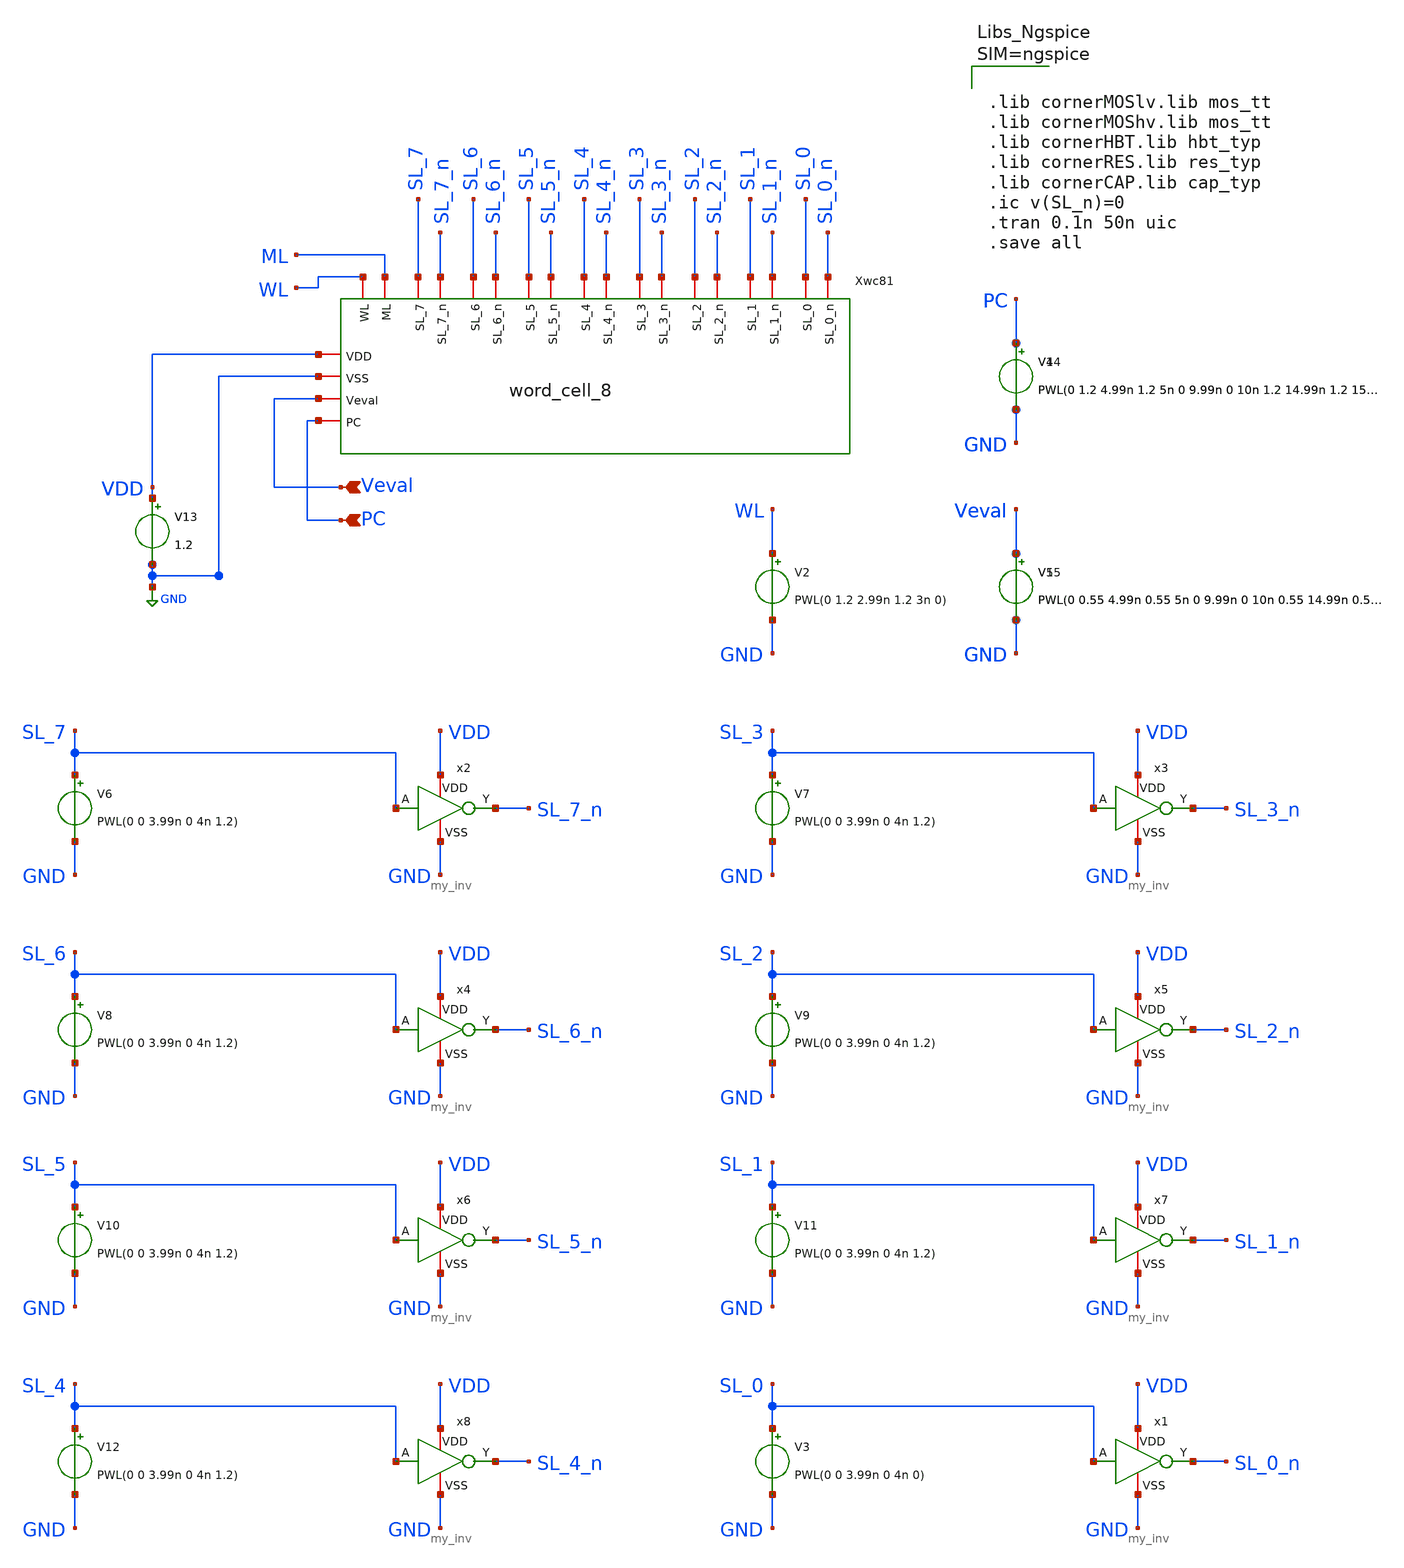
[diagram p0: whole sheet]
** sch_path: xschem/word_cell_8_TB.sch
**.subckt word_cell_8_TB PC Veval
*.ipin PC
*.ipin Veval
Xwc81 SL_3_n SL_1_n SL_2_n SL_0_n SL_7 SL_6 SL_5 SL_4 SL_3 SL_2 SL_1 SL_0 SL_7_n SL_6_n SL_5_n
+ SL_4_n WL ML VDD Veval GND PC word_cell_8
V1 VDD GND 1.2
V4 PC GND PWL(0 1.2 4.99n 1.2 5n 0 9.99n 0 10n 1.2 14.99n 1.2 15n 0 19.99n 0 20n 1.2 24.99n 1.2 25n
+ 0 29.99n 0 30n 1.2 34.99n 1.2 35n 0 39.99n 0 40n 1.2)
V5 Veval GND PWL(0 0.55 4.99n 0.55 5n 0 9.99n 0 10n 0.55 14.99n 0.55 15n 0 19.99n 0 20n 0.5 24.99n
+ 0.5 25n 0 29.99n 0 30n 0.6 34.99n 0.6 35n 0 39.99n 0 40n 0.6)
V3 SL_0 GND PWL(0 0 3.99n 0 4n 0)
V2 WL GND PWL(0 1.2 2.99n 1.2 3n 0)
x1 VDD SL_0_n SL_0 GND my_inv
V6 SL_7 GND PWL(0 0 3.99n 0 4n 1.2)
x2 VDD SL_7_n SL_7 GND my_inv
V7 SL_3 GND PWL(0 0 3.99n 0 4n 1.2)
x3 VDD SL_3_n SL_3 GND my_inv
V8 SL_6 GND PWL(0 0 3.99n 0 4n 1.2)
x4 VDD SL_6_n SL_6 GND my_inv
V9 SL_2 GND PWL(0 0 3.99n 0 4n 1.2)
x5 VDD SL_2_n SL_2 GND my_inv
V10 SL_5 GND PWL(0 0 3.99n 0 4n 1.2)
x6 VDD SL_5_n SL_5 GND my_inv
V11 SL_1 GND PWL(0 0 3.99n 0 4n 1.2)
x7 VDD SL_1_n SL_1 GND my_inv
V12 SL_4 GND PWL(0 0 3.99n 0 4n 1.2)
x8 VDD SL_4_n SL_4 GND my_inv
V13 VDD GND 1.2
V14 PC GND PWL(0 1.2 4.99n 1.2 5n 0 9.99n 0 10n 1.2 14.99n 1.2 15n 0 19.99n 0 20n 1.2 24.99n 1.2 25n
+ 0 29.99n 0 30n 1.2 34.99n 1.2 35n 0 39.99n 0 40n 1.2)
V15 Veval GND PWL(0 0.55 4.99n 0.55 5n 0 9.99n 0 10n 0.55 14.99n 0.55 15n 0 19.99n 0 20n 0.5 24.99n
+ 0.5 25n 0 29.99n 0 30n 0.6 34.99n 0.6 35n 0 39.99n 0 40n 0.6)
**** begin user architecture code



.lib cornerMOSlv.lib mos_tt
.lib cornerMOShv.lib mos_tt
.lib cornerHBT.lib hbt_typ
.lib cornerRES.lib res_typ
.lib cornerCAP.lib cap_typ
.ic v(SL_n)=0
.tran 0.1n 50n uic
.save all



**** end user architecture code
**.ends

* expanding   symbol:  word_cell_8.sym # of pins=22
** sym_path: xschem/word_cell_8.sym
** sch_path: xschem/word_cell_8.sch
.subckt word_cell_8 SL_3_n SL_1_n SL_2_n SL_0_n SL_7 SL_6 SL_5 SL_4 SL_3 SL_2 SL_1 SL_0 SL_7_n
+ SL_6_n SL_5_n SL_4_n WL ML VDD Veval VSS PC
*.iopin VSS
*.iopin Veval
*.iopin VDD
*.iopin WL
*.iopin ML
*.iopin SL_7
*.iopin SL_6
*.iopin SL_5
*.iopin SL_4
*.iopin SL_3
*.iopin SL_2
*.iopin SL_1
*.iopin SL_0
*.iopin SL_7_n
*.iopin SL_6_n
*.iopin SL_5_n
*.iopin SL_4_n
*.iopin SL_3_n
*.iopin SL_2_n
*.iopin SL_1_n
*.iopin SL_0_n
*.ipin PC
Xbc1 WL SL_7 SL_7_n VDD ML Veval VSS bitcell
Xbc2 WL SL_6 SL_6_n VDD ML Veval VSS bitcell
Xbc3 WL SL_5 SL_5_n VDD ML Veval VSS bitcell
Xbc4 WL SL_4 SL_4_n VDD ML Veval VSS bitcell
Xbc5 WL SL_3 SL_3_n VDD ML Veval VSS bitcell
Xbc6 WL SL_2 SL_2_n VDD ML Veval VSS bitcell
Xbc7 WL SL_1 SL_1_n VDD ML Veval VSS bitcell
Xbc8 WL SL_0 SL_0_n VDD ML Veval VSS bitcell
XMP0 ML PC VDD VDD sg13_lv_pmos w=2.24u l=130.00n ng=1 m=1 mm_ok=1
.ends


* expanding   symbol:  my_inv.sym # of pins=4
** sym_path: xschem/my_inv.sym
** sch_path: xschem/my_inv.sch
.subckt my_inv VDD Y A VSS
*.opin Y
*.ipin A
*.iopin VDD
*.iopin VSS
XMN0 Y A VSS VSS sg13_lv_nmos w=740.00n l=130.00n ng=1 m=1 mm_ok=1
XMP0 Y A VDD VDD sg13_lv_pmos w=1.12u l=130.00n ng=1 m=1 mm_ok=1
.ends


* expanding   symbol:  /home/designer/shared/bitcell.sym # of pins=7
** sym_path: xschem/bitcell.sym
** sch_path: xschem/bitcell.sch
.subckt bitcell WL SL SL_n VDD ML Veval VSS
*.ipin SL
*.ipin SL_n
*.ipin WL
*.iopin ML
*.ipin Veval
*.iopin VDD
*.iopin VSS
XMN1 SL WL D_n VSS sg13_lv_nmos w=740.00n l=130.00n ng=1 m=1 mm_ok=1
XMN2 SL_n WL D VSS sg13_lv_nmos w=740.00n l=130.00n ng=1 m=1 mm_ok=1
XMN3 net1 D_n SL VSS sg13_lv_nmos w=740.00n l=130.00n ng=1 m=1 mm_ok=1
XMN4 net1 D SL_n VSS sg13_lv_nmos w=740.00n l=130.00n ng=1 m=1 mm_ok=1
XMN5 ML net1 net2 VSS sg13_lv_nmos w=740.00n l=130.00n ng=1 m=1 mm_ok=1
XMN6 net2 Veval VSS VSS sg13_lv_nmos w=740.00n l=130.00n ng=1 m=1 mm_ok=1
X1 VDD D D_n VSS my_inv
X2 VDD D_n D VSS my_inv
.ends

.GLOBAL GND
.end
